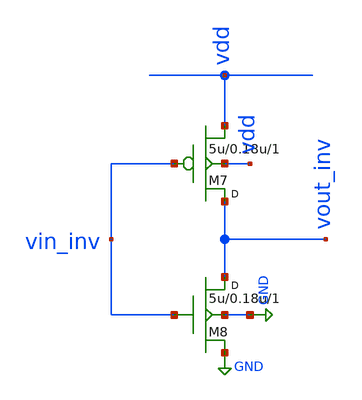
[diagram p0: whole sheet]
** sch_path: synthetic/blocks/inverter.sch
**.subckt inverter
M7 vout_inv vin_inv vdd vdd pmos w=5u l=0.18u m=1
M8 vout_inv vin_inv GND GND nmos w=5u l=0.18u m=1
**.ends
.GLOBAL GND
.end
